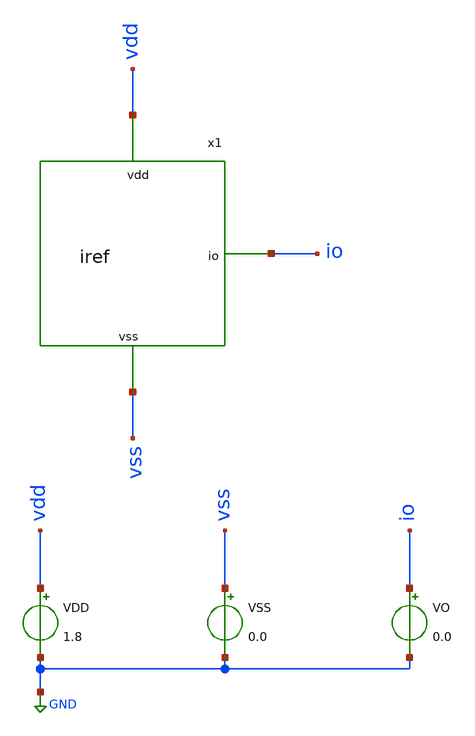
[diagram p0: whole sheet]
** sch_path: xschem/IREF/iref_tb.sch
**.subckt iref_tb
VDD vdd GND 1.8
VSS vss GND 0.0
x1 vdd io vss iref
VO io GND 0.0
**** begin user architecture code


* Include SkyWater sky130 device models
.lib /usr/share/pdk/sky130A/libs.tech/ngspice/sky130.lib.spice tt
.param mc_mm_switch=0





.param mc_mm_switch=0

.options gmin=1e-12
.options reltol=1e-5
.options abstol=1e-15
*.options rshunt = 1.0e15

.control
  op
  print i(VO)

  dc VDD 0.3 1.8 1m

  let io = i(VO)
  wrdata ../../SIM_DATA/iref_io.txt io
  plot io

  let psrr = deriv(io)/io
  wrdata ../../SIM_DATA/iref_psrr.txt io
  plot ylog abs(psrr)

.endc


**** end user architecture code
**.ends
.GLOBAL GND
.end
